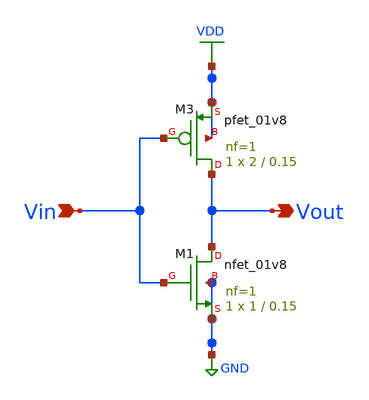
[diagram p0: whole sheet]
** sch_path: inverter.sch
**.subckt inverter Vout Vin
*.opin Vout
*.ipin Vin
XM1 Vout Vin GND GND sky130_fd_pr__nfet_01v8 L=0.15 W=1 nf=1 ad='int((nf+1)/2) * W/nf * 0.29' as='int((nf+2)/2) * W/nf * 0.29'
+ pd='2*int((nf+1)/2) * (W/nf + 0.29)' ps='2*int((nf+2)/2) * (W/nf + 0.29)' nrd='0.29 / W' nrs='0.29 / W'
+ sa=0 sb=0 sd=0 mult=1 m=1
XM3 Vout Vin VDD VDD sky130_fd_pr__pfet_01v8 L=0.15 W=2 nf=1 ad='int((nf+1)/2) * W/nf * 0.29' as='int((nf+2)/2) * W/nf * 0.29'
+ pd='2*int((nf+1)/2) * (W/nf + 0.29)' ps='2*int((nf+2)/2) * (W/nf + 0.29)' nrd='0.29 / W' nrs='0.29 / W'
+ sa=0 sb=0 sd=0 mult=1 m=1
**.ends
.GLOBAL VDD
.GLOBAL GND
.end
